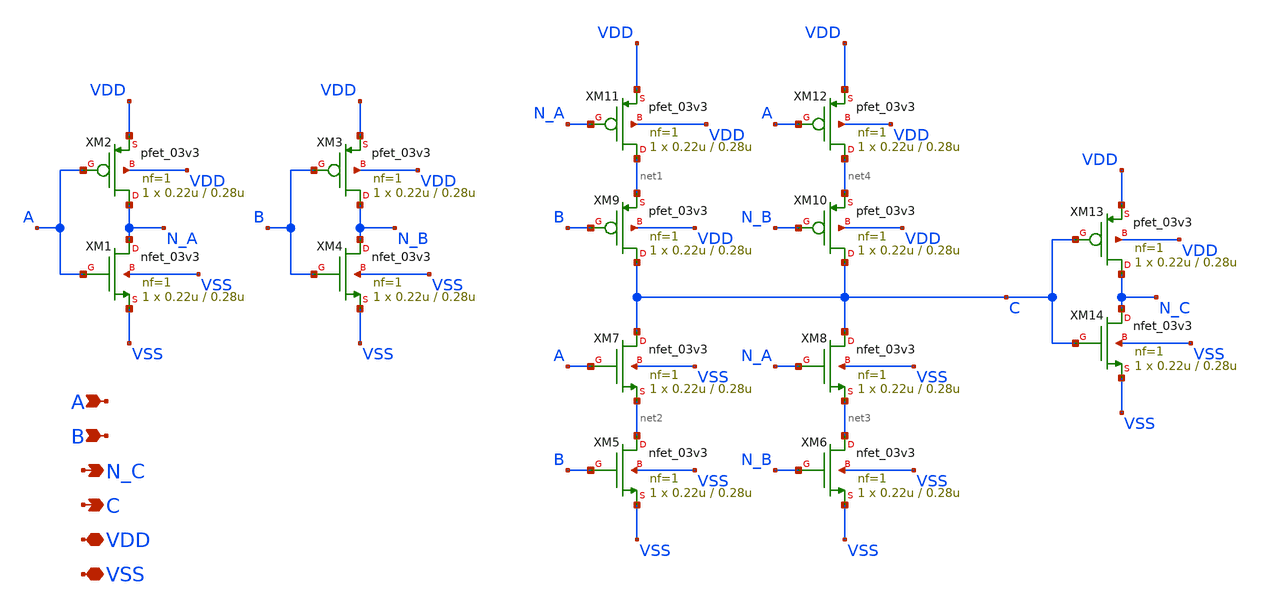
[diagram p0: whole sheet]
** sch_path: schematics/logic-gates/xor/xor.sch
**.subckt xor A B C N_C VDD VSS
*.ipin A
*.ipin B
*.opin C
*.opin N_C
*.iopin VDD
*.iopin VSS
XM1 N_A A VSS VSS nfet_03v3 L=0.28u W=0.22u nf=1 ad='int((nf+1)/2) * W/nf * 0.18u' as='int((nf+2)/2) * W/nf * 0.18u'
+ pd='2*int((nf+1)/2) * (W/nf + 0.18u)' ps='2*int((nf+2)/2) * (W/nf + 0.18u)' nrd='0.18u / W' nrs='0.18u / W'
+ sa=0 sb=0 sd=0 m=1
XM2 N_A A VDD VDD pfet_03v3 L=0.28u W=0.22u nf=1 ad='int((nf+1)/2) * W/nf * 0.18u' as='int((nf+2)/2) * W/nf * 0.18u'
+ pd='2*int((nf+1)/2) * (W/nf + 0.18u)' ps='2*int((nf+2)/2) * (W/nf + 0.18u)' nrd='0.18u / W' nrs='0.18u / W'
+ sa=0 sb=0 sd=0 m=1
XM3 N_B B VDD VDD pfet_03v3 L=0.28u W=0.22u nf=1 ad='int((nf+1)/2) * W/nf * 0.18u' as='int((nf+2)/2) * W/nf * 0.18u'
+ pd='2*int((nf+1)/2) * (W/nf + 0.18u)' ps='2*int((nf+2)/2) * (W/nf + 0.18u)' nrd='0.18u / W' nrs='0.18u / W'
+ sa=0 sb=0 sd=0 m=1
XM4 N_B B VSS VSS nfet_03v3 L=0.28u W=0.22u nf=1 ad='int((nf+1)/2) * W/nf * 0.18u' as='int((nf+2)/2) * W/nf * 0.18u'
+ pd='2*int((nf+1)/2) * (W/nf + 0.18u)' ps='2*int((nf+2)/2) * (W/nf + 0.18u)' nrd='0.18u / W' nrs='0.18u / W'
+ sa=0 sb=0 sd=0 m=1
XM5 net2 B VSS VSS nfet_03v3 L=0.28u W=0.22u nf=1 ad='int((nf+1)/2) * W/nf * 0.18u' as='int((nf+2)/2) * W/nf * 0.18u'
+ pd='2*int((nf+1)/2) * (W/nf + 0.18u)' ps='2*int((nf+2)/2) * (W/nf + 0.18u)' nrd='0.18u / W' nrs='0.18u / W'
+ sa=0 sb=0 sd=0 m=1
XM6 net3 N_B VSS VSS nfet_03v3 L=0.28u W=0.22u nf=1 ad='int((nf+1)/2) * W/nf * 0.18u' as='int((nf+2)/2) * W/nf * 0.18u'
+ pd='2*int((nf+1)/2) * (W/nf + 0.18u)' ps='2*int((nf+2)/2) * (W/nf + 0.18u)' nrd='0.18u / W' nrs='0.18u / W'
+ sa=0 sb=0 sd=0 m=1
XM7 C A net2 VSS nfet_03v3 L=0.28u W=0.22u nf=1 ad='int((nf+1)/2) * W/nf * 0.18u' as='int((nf+2)/2) * W/nf * 0.18u'
+ pd='2*int((nf+1)/2) * (W/nf + 0.18u)' ps='2*int((nf+2)/2) * (W/nf + 0.18u)' nrd='0.18u / W' nrs='0.18u / W'
+ sa=0 sb=0 sd=0 m=1
XM8 C N_A net3 VSS nfet_03v3 L=0.28u W=0.22u nf=1 ad='int((nf+1)/2) * W/nf * 0.18u' as='int((nf+2)/2) * W/nf * 0.18u'
+ pd='2*int((nf+1)/2) * (W/nf + 0.18u)' ps='2*int((nf+2)/2) * (W/nf + 0.18u)' nrd='0.18u / W' nrs='0.18u / W'
+ sa=0 sb=0 sd=0 m=1
XM9 C B net1 VDD pfet_03v3 L=0.28u W=0.22u nf=1 ad='int((nf+1)/2) * W/nf * 0.18u' as='int((nf+2)/2) * W/nf * 0.18u'
+ pd='2*int((nf+1)/2) * (W/nf + 0.18u)' ps='2*int((nf+2)/2) * (W/nf + 0.18u)' nrd='0.18u / W' nrs='0.18u / W'
+ sa=0 sb=0 sd=0 m=1
XM10 C N_B net4 VDD pfet_03v3 L=0.28u W=0.22u nf=1 ad='int((nf+1)/2) * W/nf * 0.18u' as='int((nf+2)/2) * W/nf * 0.18u'
+ pd='2*int((nf+1)/2) * (W/nf + 0.18u)' ps='2*int((nf+2)/2) * (W/nf + 0.18u)' nrd='0.18u / W' nrs='0.18u / W'
+ sa=0 sb=0 sd=0 m=1
XM11 net1 N_A VDD VDD pfet_03v3 L=0.28u W=0.22u nf=1 ad='int((nf+1)/2) * W/nf * 0.18u' as='int((nf+2)/2) * W/nf * 0.18u'
+ pd='2*int((nf+1)/2) * (W/nf + 0.18u)' ps='2*int((nf+2)/2) * (W/nf + 0.18u)' nrd='0.18u / W' nrs='0.18u / W'
+ sa=0 sb=0 sd=0 m=1
XM12 net4 A VDD VDD pfet_03v3 L=0.28u W=0.22u nf=1 ad='int((nf+1)/2) * W/nf * 0.18u' as='int((nf+2)/2) * W/nf * 0.18u'
+ pd='2*int((nf+1)/2) * (W/nf + 0.18u)' ps='2*int((nf+2)/2) * (W/nf + 0.18u)' nrd='0.18u / W' nrs='0.18u / W'
+ sa=0 sb=0 sd=0 m=1
XM13 N_C C VDD VDD pfet_03v3 L=0.28u W=0.22u nf=1 ad='int((nf+1)/2) * W/nf * 0.18u' as='int((nf+2)/2) * W/nf * 0.18u'
+ pd='2*int((nf+1)/2) * (W/nf + 0.18u)' ps='2*int((nf+2)/2) * (W/nf + 0.18u)' nrd='0.18u / W' nrs='0.18u / W'
+ sa=0 sb=0 sd=0 m=1
XM14 N_C C VSS VSS nfet_03v3 L=0.28u W=0.22u nf=1 ad='int((nf+1)/2) * W/nf * 0.18u' as='int((nf+2)/2) * W/nf * 0.18u'
+ pd='2*int((nf+1)/2) * (W/nf + 0.18u)' ps='2*int((nf+2)/2) * (W/nf + 0.18u)' nrd='0.18u / W' nrs='0.18u / W'
+ sa=0 sb=0 sd=0 m=1
**.ends
.end
